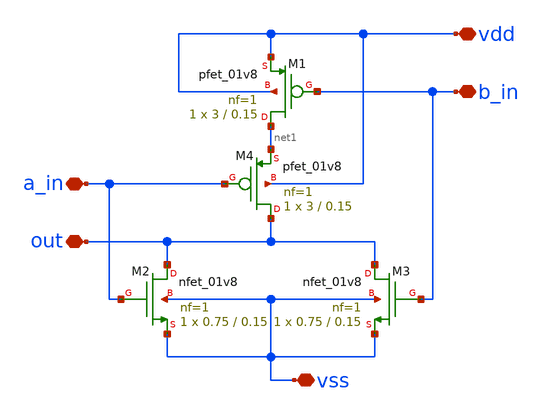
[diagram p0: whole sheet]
** sch_path: design/blocks/norgate/schematic/norgate.sch
**.subckt norgate a_in out vss vdd b_in
*.iopin a_in
*.iopin out
*.iopin vss
*.iopin vdd
*.iopin b_in
XM1 net1 b_in vdd vdd sky130_fd_pr__pfet_01v8 L=0.15 W=3 nf=1 ad='int((nf+1)/2) * W/nf * 0.29' as='int((nf+2)/2) * W/nf * 0.29'
+ pd='2*int((nf+1)/2) * (W/nf + 0.29)' ps='2*int((nf+2)/2) * (W/nf + 0.29)' nrd='0.29 / W' nrs='0.29 / W'
+ sa=0 sb=0 sd=0 mult=1 m=1
XM2 out a_in vss vss sky130_fd_pr__nfet_01v8 L=0.15 W=0.75 nf=1 ad='int((nf+1)/2) * W/nf * 0.29' as='int((nf+2)/2) * W/nf * 0.29'
+ pd='2*int((nf+1)/2) * (W/nf + 0.29)' ps='2*int((nf+2)/2) * (W/nf + 0.29)' nrd='0.29 / W' nrs='0.29 / W'
+ sa=0 sb=0 sd=0 mult=1 m=1
XM3 out b_in vss vss sky130_fd_pr__nfet_01v8 L=0.15 W=0.75 nf=1 ad='int((nf+1)/2) * W/nf * 0.29' as='int((nf+2)/2) * W/nf * 0.29'
+ pd='2*int((nf+1)/2) * (W/nf + 0.29)' ps='2*int((nf+2)/2) * (W/nf + 0.29)' nrd='0.29 / W' nrs='0.29 / W'
+ sa=0 sb=0 sd=0 mult=1 m=1
XM4 out a_in net1 vdd sky130_fd_pr__pfet_01v8 L=0.15 W=3 nf=1 ad='int((nf+1)/2) * W/nf * 0.29' as='int((nf+2)/2) * W/nf * 0.29'
+ pd='2*int((nf+1)/2) * (W/nf + 0.29)' ps='2*int((nf+2)/2) * (W/nf + 0.29)' nrd='0.29 / W' nrs='0.29 / W'
+ sa=0 sb=0 sd=0 mult=1 m=1
**.ends
.end
